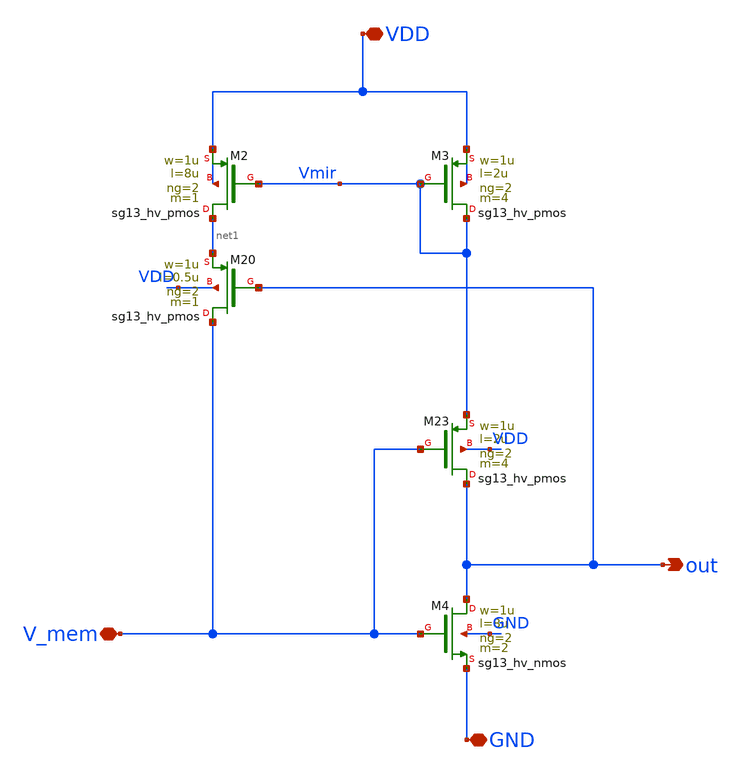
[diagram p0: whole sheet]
** sch_path: xschem/FB_system.sch
**.subckt FB_system out V_mem VDD GND
*.opin out
*.iopin V_mem
*.iopin VDD
*.iopin GND
XM3 Vmir Vmir VDD VDD sg13_hv_pmos w=1u l=2u ng=2 m=4 mm_ok=1
XM20 V_mem out net1 VDD sg13_hv_pmos w=1u l=0.5u ng=2 m=1 mm_ok=1
XM2 net1 Vmir VDD VDD sg13_hv_pmos w=1u l=8u ng=2 m=1 mm_ok=1
XM23 out V_mem Vmir VDD sg13_hv_pmos w=1u l=2u ng=2 m=4 mm_ok=1
XM4 out V_mem GND GND sg13_hv_nmos w=1u l=8u ng=2 m=2 mm_ok=1
**.ends
.end
